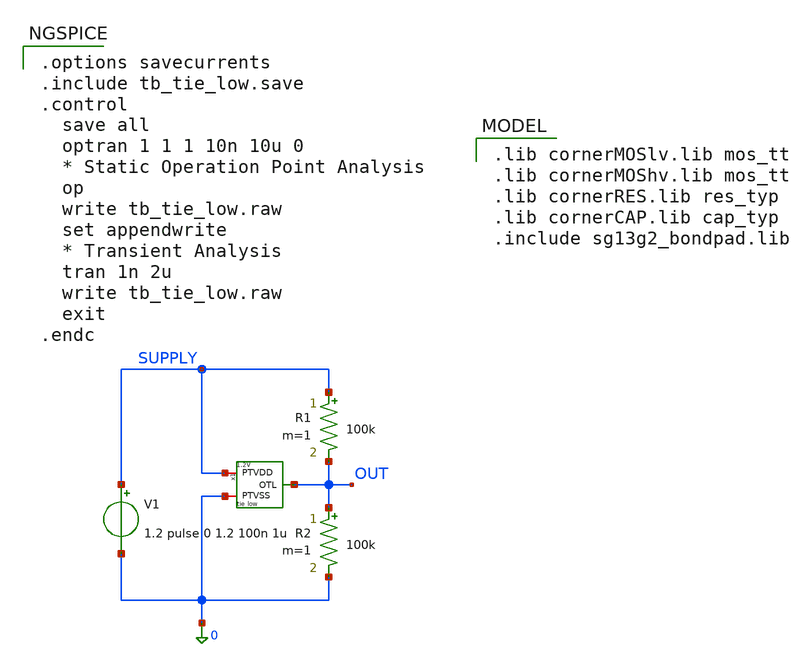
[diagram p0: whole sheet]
** sch_path: xschem/tb_tie_low.sch
**.subckt tb_tie_low
x1 SUPPLY OUT 0 tie_low
V1 SUPPLY 0 1.2 pulse 0 1.2 100n 1u
R1 SUPPLY OUT 100k m=1
R2 OUT 0 100k m=1
**** begin user architecture code

.options savecurrents
.include tb_tie_low.save
.control
  save all
  optran 1 1 1 10n 10u 0
  * Static Operation Point Analysis
  op
  write tb_tie_low.raw
  set appendwrite
  * Transient Analysis
  tran 1n 2u
  write tb_tie_low.raw
  exit
.endc



.lib cornerMOSlv.lib mos_tt
.lib cornerMOShv.lib mos_tt
.lib cornerRES.lib res_typ
.lib cornerCAP.lib cap_typ
.include sg13g2_bondpad.lib


**** end user architecture code
**.ends

* expanding   symbol:  tie_low.sym # of pins=3
** sym_path: xschem/tie_low.sym
** sch_path: xschem/tie_low.sch
.subckt tie_low PTVDD OTL PTVSS
*.iopin PTVDD
*.iopin PTVSS
*.opin OTL
XMN0 net2 net3 PTVSS PTVSS sg13_lv_nmos w=0.38u l=0.13u ng=1 m=1 mm_ok=1
XMP1 net1 net2 PTVDD PTVDD sg13_lv_pmos w=1u l=0.13u ng=1 m=1 mm_ok=1
XMN1 OTL net1 PTVSS PTVSS sg13_lv_nmos w=0.8u l=0.13u ng=1 m=1 mm_ok=1
XMP0 net3 net3 PTVDD PTVDD sg13_lv_pmos w=0.3u l=0.13u ng=1 m=1 mm_ok=1
.ends

.end
